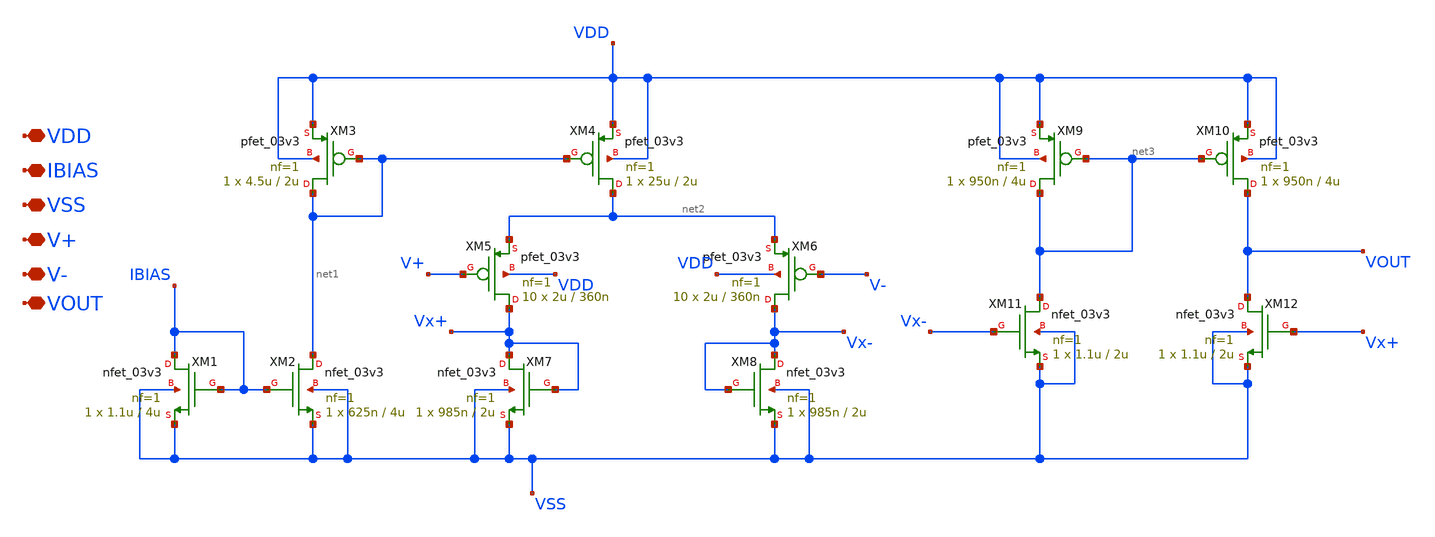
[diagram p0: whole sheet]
** sch_path: designs/static_comparator/xschem/static_comparator.sch
**.subckt static_comparator IBIAS VSS VDD V+ V- VOUT
*.iopin IBIAS
*.iopin VSS
*.iopin VDD
*.iopin V+
*.iopin V-
*.iopin VOUT
XM1 IBIAS IBIAS VSS VSS nfet_03v3 L=4u W=1.1u nf=1 ad='int((nf+1)/2) * W/nf * 0.18u' as='int((nf+2)/2) * W/nf * 0.18u'
+ pd='2*int((nf+1)/2) * (W/nf + 0.18u)' ps='2*int((nf+2)/2) * (W/nf + 0.18u)' nrd='0.18u / W' nrs='0.18u / W'
+ sa=0 sb=0 sd=0 m=1
XM3 net1 net1 VDD VDD pfet_03v3 L=2u W=4.5u nf=1 ad='int((nf+1)/2) * W/nf * 0.18u' as='int((nf+2)/2) * W/nf * 0.18u'
+ pd='2*int((nf+1)/2) * (W/nf + 0.18u)' ps='2*int((nf+2)/2) * (W/nf + 0.18u)' nrd='0.18u / W' nrs='0.18u / W'
+ sa=0 sb=0 sd=0 m=1
XM2 net1 IBIAS VSS VSS nfet_03v3 L=4u W=625n nf=1 ad='int((nf+1)/2) * W/nf * 0.18u' as='int((nf+2)/2) * W/nf * 0.18u'
+ pd='2*int((nf+1)/2) * (W/nf + 0.18u)' ps='2*int((nf+2)/2) * (W/nf + 0.18u)' nrd='0.18u / W' nrs='0.18u / W'
+ sa=0 sb=0 sd=0 m=1
XM4 net2 net1 VDD VDD pfet_03v3 L=2u W=25u nf=1 ad='int((nf+1)/2) * W/nf * 0.18u' as='int((nf+2)/2) * W/nf * 0.18u'
+ pd='2*int((nf+1)/2) * (W/nf + 0.18u)' ps='2*int((nf+2)/2) * (W/nf + 0.18u)' nrd='0.18u / W' nrs='0.18u / W'
+ sa=0 sb=0 sd=0 m=1
XM5 Vx+ V+ net2 VDD pfet_03v3 L=360n W=2u nf=1 ad='int((nf+1)/2) * W/nf * 0.18u' as='int((nf+2)/2) * W/nf * 0.18u'
+ pd='2*int((nf+1)/2) * (W/nf + 0.18u)' ps='2*int((nf+2)/2) * (W/nf + 0.18u)' nrd='0.18u / W' nrs='0.18u / W'
+ sa=0 sb=0 sd=0 m=10
XM7 Vx+ Vx+ VSS VSS nfet_03v3 L=2u W=985n nf=1 ad='int((nf+1)/2) * W/nf * 0.18u' as='int((nf+2)/2) * W/nf * 0.18u'
+ pd='2*int((nf+1)/2) * (W/nf + 0.18u)' ps='2*int((nf+2)/2) * (W/nf + 0.18u)' nrd='0.18u / W' nrs='0.18u / W'
+ sa=0 sb=0 sd=0 m=1
XM6 Vx- V- net2 VDD pfet_03v3 L=360n W=2u nf=1 ad='int((nf+1)/2) * W/nf * 0.18u' as='int((nf+2)/2) * W/nf * 0.18u'
+ pd='2*int((nf+1)/2) * (W/nf + 0.18u)' ps='2*int((nf+2)/2) * (W/nf + 0.18u)' nrd='0.18u / W' nrs='0.18u / W'
+ sa=0 sb=0 sd=0 m=10
XM8 Vx- Vx- VSS VSS nfet_03v3 L=2u W=985n nf=1 ad='int((nf+1)/2) * W/nf * 0.18u' as='int((nf+2)/2) * W/nf * 0.18u'
+ pd='2*int((nf+1)/2) * (W/nf + 0.18u)' ps='2*int((nf+2)/2) * (W/nf + 0.18u)' nrd='0.18u / W' nrs='0.18u / W'
+ sa=0 sb=0 sd=0 m=1
XM9 net3 net3 VDD VDD pfet_03v3 L=4u W=950n nf=1 ad='int((nf+1)/2) * W/nf * 0.18u' as='int((nf+2)/2) * W/nf * 0.18u'
+ pd='2*int((nf+1)/2) * (W/nf + 0.18u)' ps='2*int((nf+2)/2) * (W/nf + 0.18u)' nrd='0.18u / W' nrs='0.18u / W'
+ sa=0 sb=0 sd=0 m=1
XM10 VOUT net3 VDD VDD pfet_03v3 L=4u W=950n nf=1 ad='int((nf+1)/2) * W/nf * 0.18u' as='int((nf+2)/2) * W/nf * 0.18u'
+ pd='2*int((nf+1)/2) * (W/nf + 0.18u)' ps='2*int((nf+2)/2) * (W/nf + 0.18u)' nrd='0.18u / W' nrs='0.18u / W'
+ sa=0 sb=0 sd=0 m=1
XM11 net3 Vx- VSS VSS nfet_03v3 L=2u W=1.1u nf=1 ad='int((nf+1)/2) * W/nf * 0.18u' as='int((nf+2)/2) * W/nf * 0.18u'
+ pd='2*int((nf+1)/2) * (W/nf + 0.18u)' ps='2*int((nf+2)/2) * (W/nf + 0.18u)' nrd='0.18u / W' nrs='0.18u / W'
+ sa=0 sb=0 sd=0 m=1
XM12 VOUT Vx+ VSS VSS nfet_03v3 L=2u W=1.1u nf=1 ad='int((nf+1)/2) * W/nf * 0.18u' as='int((nf+2)/2) * W/nf * 0.18u'
+ pd='2*int((nf+1)/2) * (W/nf + 0.18u)' ps='2*int((nf+2)/2) * (W/nf + 0.18u)' nrd='0.18u / W' nrs='0.18u / W'
+ sa=0 sb=0 sd=0 m=1
**.ends
.end
